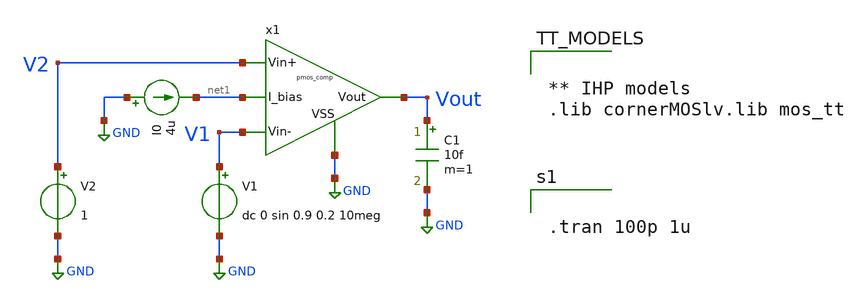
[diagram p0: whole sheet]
** sch_path: SSDOR_1.2V_v4/components/pmos_comp/tb_pmos_comp.sch
**.subckt tb_pmos_comp
x1 V1 V2 Vout net1 GND pmos_comp
V1 V1 GND dc 0 sin 0.9 0.2 10meg
I0 GND net1 4u
V2 V2 GND 1
C1 Vout GND 10f m=1
**** begin user architecture code


.tran 100p 1u




** IHP models
.lib cornerMOSlv.lib mos_tt


**** end user architecture code
**.ends
.GLOBAL GND
.end
